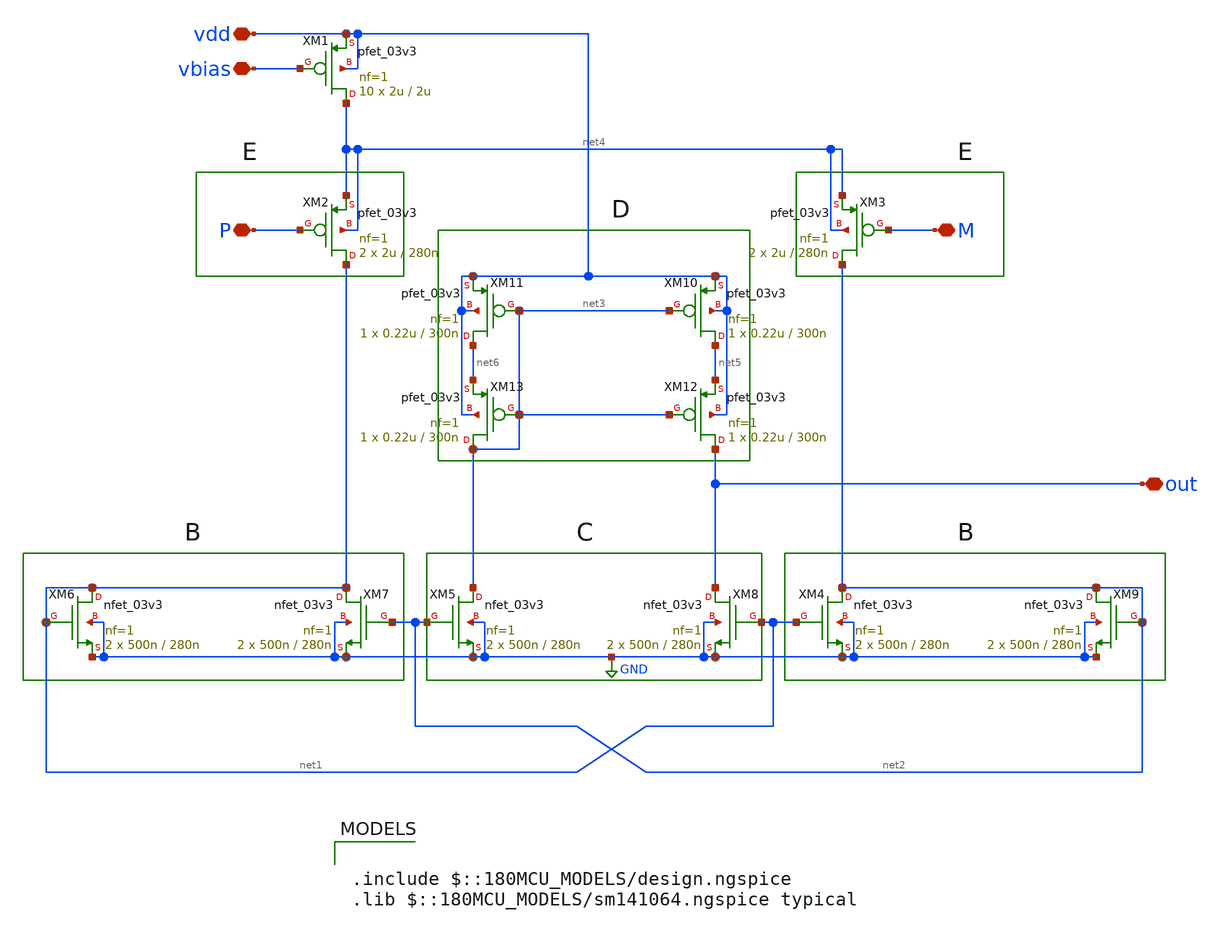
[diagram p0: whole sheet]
** sch_path: Clock_Reference/symbols_clock/comparator.sch
**.subckt comparator out M P vbias vdd
*.iopin out
*.iopin M
*.iopin P
*.iopin vbias
*.iopin vdd
XM1 net4 vbias vdd vdd pfet_03v3 L=2u W=2u nf=1 ad='int((nf+1)/2) * W/nf * 0.18u' as='int((nf+2)/2) * W/nf * 0.18u'
+ pd='2*int((nf+1)/2) * (W/nf + 0.18u)' ps='2*int((nf+2)/2) * (W/nf + 0.18u)' nrd='0.18u / W' nrs='0.18u / W'
+ sa=0 sb=0 sd=0 m=10
XM2 net1 P net4 net4 pfet_03v3 L=280n W=2u nf=1 ad='int((nf+1)/2) * W/nf * 0.18u' as='int((nf+2)/2) * W/nf * 0.18u'
+ pd='2*int((nf+1)/2) * (W/nf + 0.18u)' ps='2*int((nf+2)/2) * (W/nf + 0.18u)' nrd='0.18u / W' nrs='0.18u / W'
+ sa=0 sb=0 sd=0 m=2
XM3 net2 M net4 net4 pfet_03v3 L=280n W=2u nf=1 ad='int((nf+1)/2) * W/nf * 0.18u' as='int((nf+2)/2) * W/nf * 0.18u'
+ pd='2*int((nf+1)/2) * (W/nf + 0.18u)' ps='2*int((nf+2)/2) * (W/nf + 0.18u)' nrd='0.18u / W' nrs='0.18u / W'
+ sa=0 sb=0 sd=0 m=2
XM4 net2 net1 GND GND nfet_03v3 L=280n W=500n nf=1 ad='int((nf+1)/2) * W/nf * 0.18u' as='int((nf+2)/2) * W/nf * 0.18u'
+ pd='2*int((nf+1)/2) * (W/nf + 0.18u)' ps='2*int((nf+2)/2) * (W/nf + 0.18u)' nrd='0.18u / W' nrs='0.18u / W'
+ sa=0 sb=0 sd=0 m=2
XM5 net3 net2 GND GND nfet_03v3 L=280n W=500n nf=1 ad='int((nf+1)/2) * W/nf * 0.18u' as='int((nf+2)/2) * W/nf * 0.18u'
+ pd='2*int((nf+1)/2) * (W/nf + 0.18u)' ps='2*int((nf+2)/2) * (W/nf + 0.18u)' nrd='0.18u / W' nrs='0.18u / W'
+ sa=0 sb=0 sd=0 m=2
XM6 net1 net1 GND GND nfet_03v3 L=280n W=500n nf=1 ad='int((nf+1)/2) * W/nf * 0.18u' as='int((nf+2)/2) * W/nf * 0.18u'
+ pd='2*int((nf+1)/2) * (W/nf + 0.18u)' ps='2*int((nf+2)/2) * (W/nf + 0.18u)' nrd='0.18u / W' nrs='0.18u / W'
+ sa=0 sb=0 sd=0 m=2
XM7 net1 net2 GND GND nfet_03v3 L=280n W=500n nf=1 ad='int((nf+1)/2) * W/nf * 0.18u' as='int((nf+2)/2) * W/nf * 0.18u'
+ pd='2*int((nf+1)/2) * (W/nf + 0.18u)' ps='2*int((nf+2)/2) * (W/nf + 0.18u)' nrd='0.18u / W' nrs='0.18u / W'
+ sa=0 sb=0 sd=0 m=2
XM8 out net1 GND GND nfet_03v3 L=280n W=500n nf=1 ad='int((nf+1)/2) * W/nf * 0.18u' as='int((nf+2)/2) * W/nf * 0.18u'
+ pd='2*int((nf+1)/2) * (W/nf + 0.18u)' ps='2*int((nf+2)/2) * (W/nf + 0.18u)' nrd='0.18u / W' nrs='0.18u / W'
+ sa=0 sb=0 sd=0 m=2
XM9 net2 net2 GND GND nfet_03v3 L=280n W=500n nf=1 ad='int((nf+1)/2) * W/nf * 0.18u' as='int((nf+2)/2) * W/nf * 0.18u'
+ pd='2*int((nf+1)/2) * (W/nf + 0.18u)' ps='2*int((nf+2)/2) * (W/nf + 0.18u)' nrd='0.18u / W' nrs='0.18u / W'
+ sa=0 sb=0 sd=0 m=2
XM10 net5 net3 vdd vdd pfet_03v3 L=300n W=0.22u nf=1 ad='int((nf+1)/2) * W/nf * 0.18u' as='int((nf+2)/2) * W/nf * 0.18u'
+ pd='2*int((nf+1)/2) * (W/nf + 0.18u)' ps='2*int((nf+2)/2) * (W/nf + 0.18u)' nrd='0.18u / W' nrs='0.18u / W'
+ sa=0 sb=0 sd=0 m=1
XM11 net6 net3 vdd vdd pfet_03v3 L=300n W=0.22u nf=1 ad='int((nf+1)/2) * W/nf * 0.18u' as='int((nf+2)/2) * W/nf * 0.18u'
+ pd='2*int((nf+1)/2) * (W/nf + 0.18u)' ps='2*int((nf+2)/2) * (W/nf + 0.18u)' nrd='0.18u / W' nrs='0.18u / W'
+ sa=0 sb=0 sd=0 m=1
XM12 out net3 net5 vdd pfet_03v3 L=300n W=0.22u nf=1 ad='int((nf+1)/2) * W/nf * 0.18u' as='int((nf+2)/2) * W/nf * 0.18u'
+ pd='2*int((nf+1)/2) * (W/nf + 0.18u)' ps='2*int((nf+2)/2) * (W/nf + 0.18u)' nrd='0.18u / W' nrs='0.18u / W'
+ sa=0 sb=0 sd=0 m=1
XM13 net3 net3 net6 vdd pfet_03v3 L=300n W=0.22u nf=1 ad='int((nf+1)/2) * W/nf * 0.18u' as='int((nf+2)/2) * W/nf * 0.18u'
+ pd='2*int((nf+1)/2) * (W/nf + 0.18u)' ps='2*int((nf+2)/2) * (W/nf + 0.18u)' nrd='0.18u / W' nrs='0.18u / W'
+ sa=0 sb=0 sd=0 m=1
**** begin user architecture code

.include $::180MCU_MODELS/design.ngspice
.lib $::180MCU_MODELS/sm141064.ngspice typical

**** end user architecture code
**.ends
.GLOBAL GND
.end
